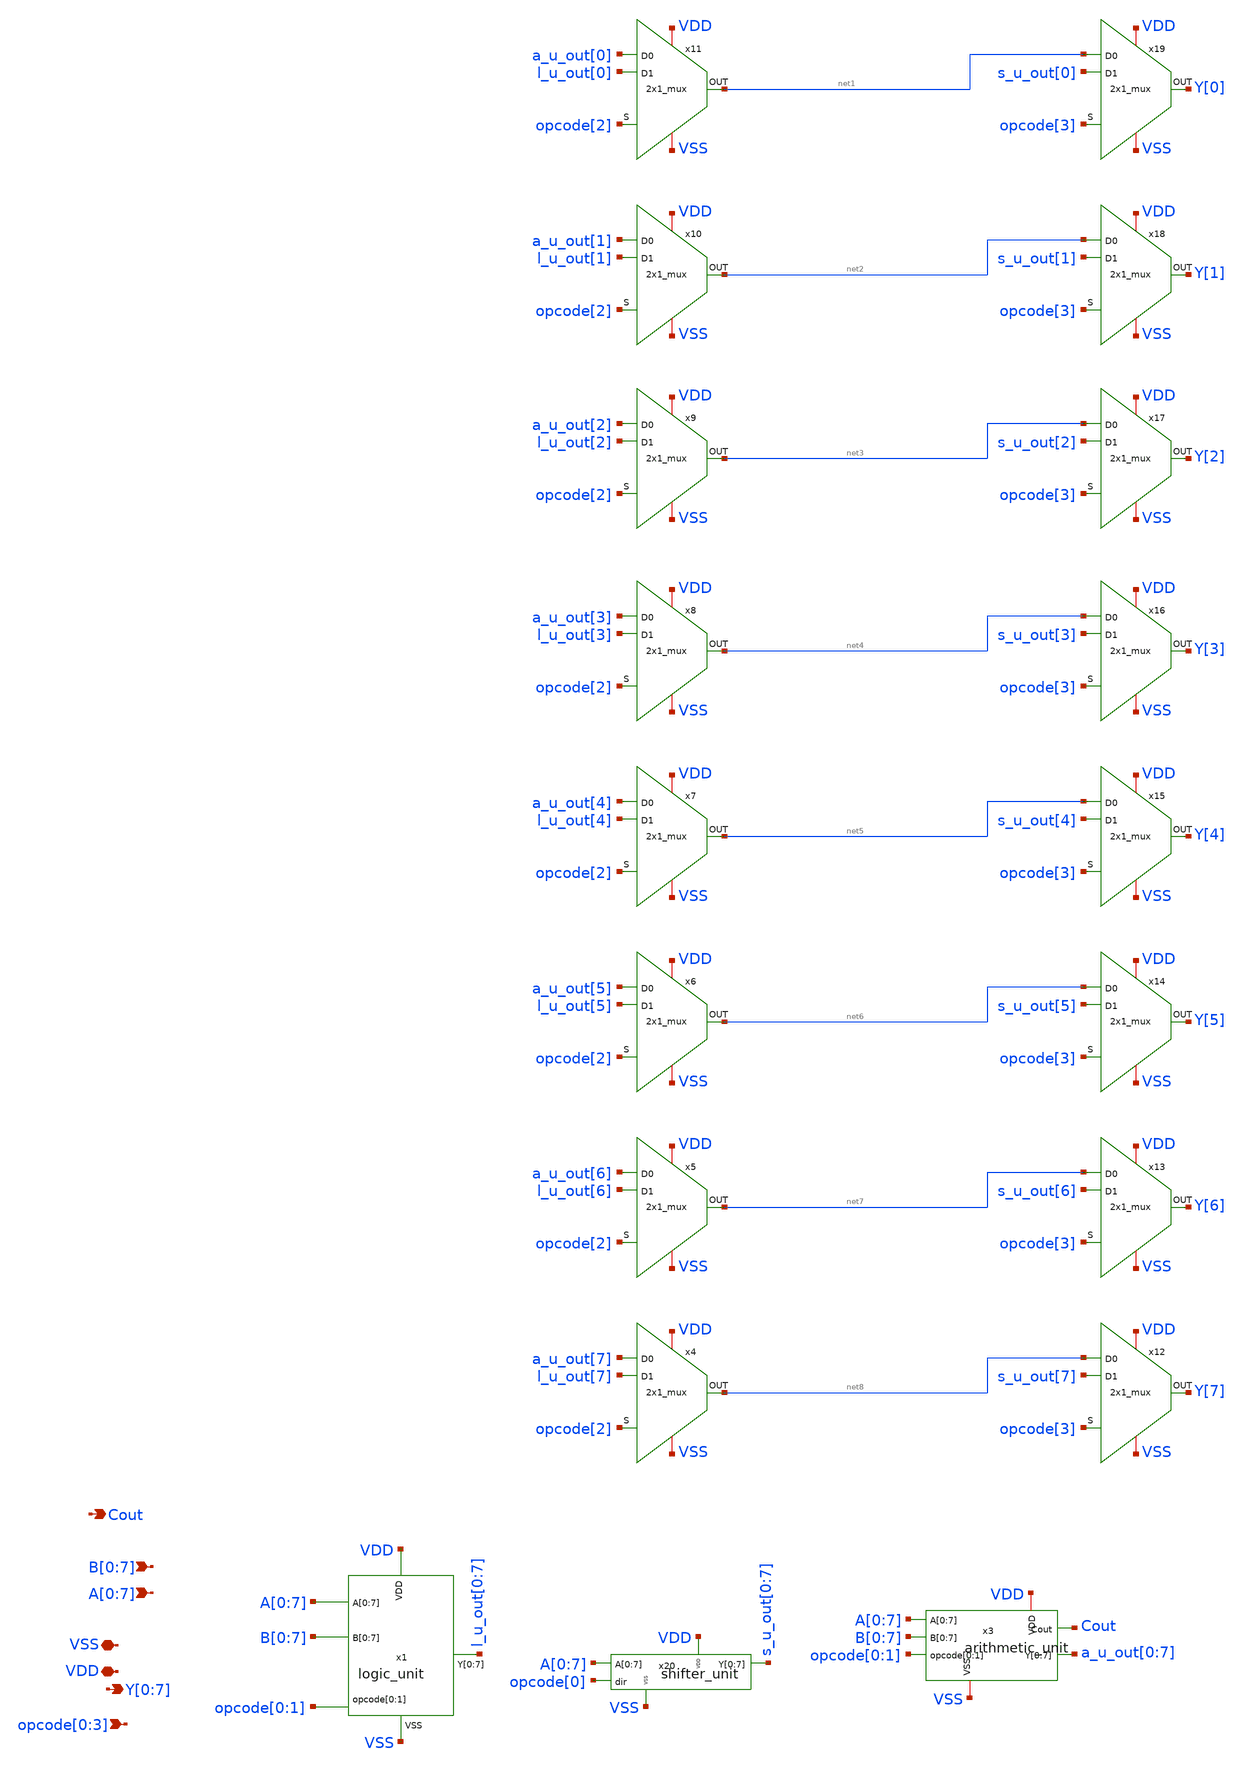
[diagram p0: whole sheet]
** sch_path: design/ALU/control_unit.sch
**.subckt control_unit B[0],B[1],B[2],B[3],B[4],B[5],B[6],B[7]
*+ A[0],A[1],A[2],A[3],A[4],A[5],A[6],A[7] Y[0],Y[1],Y[2],Y[3],Y[4],Y[5],Y[6],Y[7] VDD VSS opcode[0],opcode[1],opcode[2],opcode[3] Cout
*.ipin B[0],B[1],B[2],B[3],B[4],B[5],B[6],B[7]
*.ipin A[0],A[1],A[2],A[3],A[4],A[5],A[6],A[7]
*.opin Y[0],Y[1],Y[2],Y[3],Y[4],Y[5],Y[6],Y[7]
*.iopin VDD
*.iopin VSS
*.ipin opcode[0],opcode[1],opcode[2],opcode[3]
*.opin Cout
x1 B[0] B[1] B[2] B[3] B[4] B[5] B[6] B[7] l_u_out[0] l_u_out[1] l_u_out[2] l_u_out[3] l_u_out[4]
+ l_u_out[5] l_u_out[6] l_u_out[7] VDD VSS opcode[0] opcode[1] A[0] A[1] A[2] A[3] A[4] A[5] A[6] A[7]
+ logic_unit
x3 A[0] A[1] A[2] A[3] A[4] A[5] A[6] A[7] B[0] B[1] B[2] B[3] B[4] B[5] B[6] B[7] opcode[0]
+ opcode[1] a_u_out[0] a_u_out[1] a_u_out[2] a_u_out[3] a_u_out[4] a_u_out[5] a_u_out[6] a_u_out[7] Cout VSS
+ VDD arithmetic_unit
x4 VSS VDD opcode[2] a_u_out[7] l_u_out[7] net8 2x1_mux
x5 VSS VDD opcode[2] a_u_out[6] l_u_out[6] net7 2x1_mux
x6 VSS VDD opcode[2] a_u_out[5] l_u_out[5] net6 2x1_mux
x7 VSS VDD opcode[2] a_u_out[4] l_u_out[4] net5 2x1_mux
x8 VSS VDD opcode[2] a_u_out[3] l_u_out[3] net4 2x1_mux
x9 VSS VDD opcode[2] a_u_out[2] l_u_out[2] net3 2x1_mux
x10 VSS VDD opcode[2] a_u_out[1] l_u_out[1] net2 2x1_mux
x11 VSS VDD opcode[2] a_u_out[0] l_u_out[0] net1 2x1_mux
x12 VSS VDD opcode[3] net8 s_u_out[7] Y[7] 2x1_mux
x13 VSS VDD opcode[3] net7 s_u_out[6] Y[6] 2x1_mux
x14 VSS VDD opcode[3] net6 s_u_out[5] Y[5] 2x1_mux
x15 VSS VDD opcode[3] net5 s_u_out[4] Y[4] 2x1_mux
x16 VSS VDD opcode[3] net4 s_u_out[3] Y[3] 2x1_mux
x17 VSS VDD opcode[3] net3 s_u_out[2] Y[2] 2x1_mux
x18 VSS VDD opcode[3] net2 s_u_out[1] Y[1] 2x1_mux
x19 VSS VDD opcode[3] net1 s_u_out[0] Y[0] 2x1_mux
x20 A[0] A[1] A[2] A[3] A[4] A[5] A[6] A[7] s_u_out[0] s_u_out[1] s_u_out[2] s_u_out[3] s_u_out[4]
+ s_u_out[5] s_u_out[6] s_u_out[7] opcode[0] VSS VDD shifter_unit
**.ends
.end
